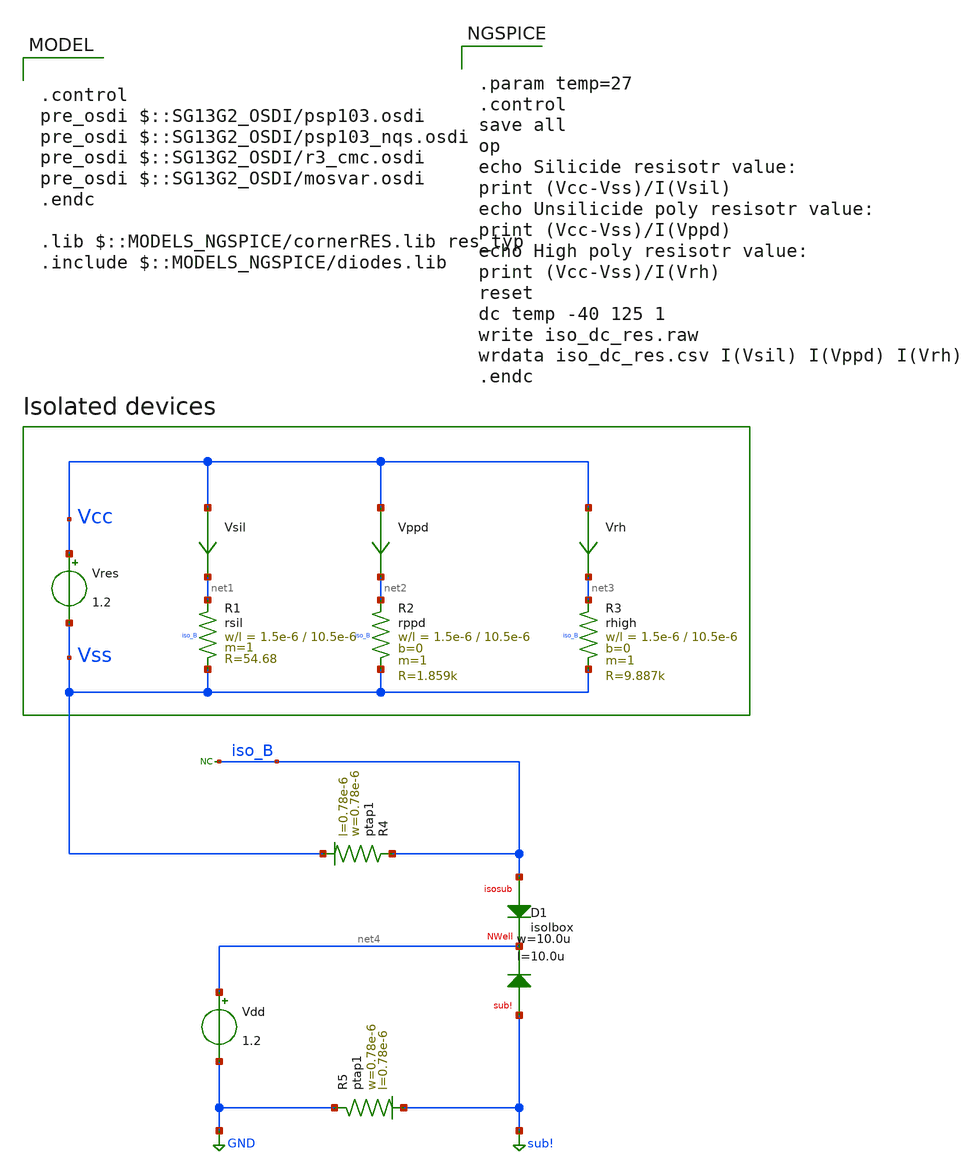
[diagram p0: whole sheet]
** sch_path: ihp-sg13g2/xschem_libs/sg13g2_tests/iso_dc_res/schematic/iso_dc_res.sch
* Copyright 2023 IHP PDK Authors
**.subckt iso_dc_res
Vres Vcc Vss 1.2
Vsil Vcc net1 0
.save i(vsil)
Vppd Vcc net2 0
.save i(vppd)
Vrh Vcc net3 0
.save i(vrh)
XR1 net1 Vss iso_B rsil w=1.5e-6 l=10.5e-6 m=1 mm_ok=1
XR2 net2 Vss iso_B rppd w=1.5e-6 l=10.5e-6 m=1 b=0 mm_ok=1
XR3 net3 Vss iso_B rhigh w=1.5e-6 l=10.5e-6 m=1 b=0 mm_ok=1
XR5 GND sub! ptap1 R=262.8 w=0.78e-6 l=0.78e-6
Vdd net4 GND 1.2
XD1 iso_B net4 sub! isolbox l=10.0u w=10.0u
* noconn iso_B
XR4 iso_B Vss ptap1 R=262.8 w=0.78e-6 l=0.78e-6
**** begin user architecture code

.control
pre_osdi $::SG13G2_OSDI/psp103.osdi
pre_osdi $::SG13G2_OSDI/psp103_nqs.osdi
pre_osdi $::SG13G2_OSDI/r3_cmc.osdi
pre_osdi $::SG13G2_OSDI/mosvar.osdi
.endc

.lib $::MODELS_NGSPICE/cornerRES.lib res_typ
.include $::MODELS_NGSPICE/diodes.lib



.param temp=27
.control
save all
op
echo Silicide resisotr value:
print (Vcc-Vss)/I(Vsil)
echo Unsilicide poly resisotr value:
print (Vcc-Vss)/I(Vppd)
echo High poly resisotr value:
print (Vcc-Vss)/I(Vrh)
reset
dc temp -40 125 1
write iso_dc_res.raw
wrdata iso_dc_res.csv I(Vsil) I(Vppd) I(Vrh)
.endc


**** end user architecture code
**.ends
.GLOBAL GND
.GLOBAL sub!
.end
